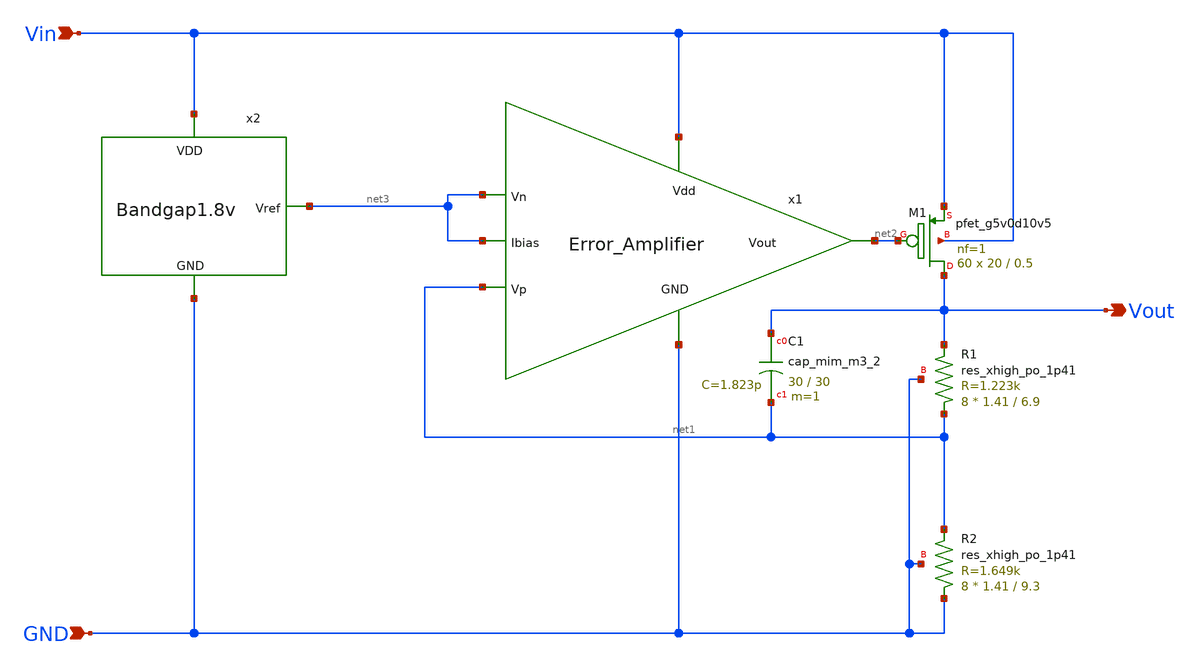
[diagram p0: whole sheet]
** sch_path: Analog_blocks/Analog_Blocks/LDO/Schematic/LDO_Miller_1.8v/LDO_Miller_OTA_1.8v.sch
**.subckt LDO_Miller_OTA_1.8v Vin GND Vout
*.ipin Vin
*.ipin GND
*.opin Vout
XC1 Vout net1 sky130_fd_pr__cap_mim_m3_2 W=30 L=30 MF=1 m=1
XM1 Vout net2 Vin Vin sky130_fd_pr__pfet_g5v0d10v5 L=0.5 W=20 nf=1 ad='int((nf+1)/2) * W/nf * 0.29' as='int((nf+2)/2) * W/nf * 0.29'
+ pd='2*int((nf+1)/2) * (W/nf + 0.29)' ps='2*int((nf+2)/2) * (W/nf + 0.29)' nrd='0.29 / W' nrs='0.29 / W'
+ sa=0 sb=0 sd=0 mult=60 m=60
XR1 net1 Vout GND sky130_fd_pr__res_xhigh_po_1p41 L=6.9 mult=8 m=8
XR2 GND net1 GND sky130_fd_pr__res_xhigh_po_1p41 L=9.3 mult=8 m=8
x1 Vin net3 net1 net2 net3 GND Error_Amplifier
x2 net3 Vin GND Bandgap1.8v
**.ends
.end
